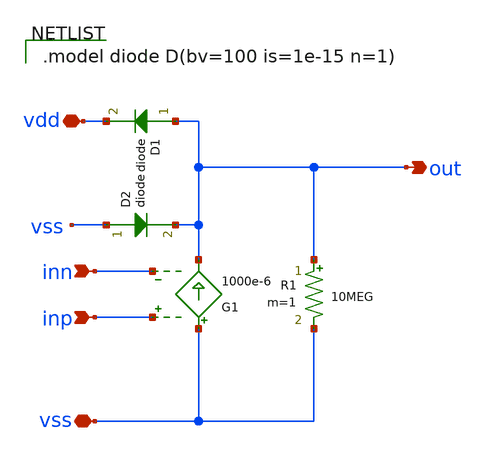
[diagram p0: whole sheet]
** sch_path: 10_xschem/ota1.sch
**.subckt ota1 inn out vss inp vdd
*.ipin inn
*.opin out
*.iopin vss
*.ipin inp
*.iopin vdd
G1 vss out inp inn 1000e-6
R1 out vss 10MEG m=1
D1 out vdd diode area=1
D2 vss out diode area=1
**** begin user architecture code

.model diode D(bv=100 is=1e-15 n=1)

**** end user architecture code
**.ends
.end
